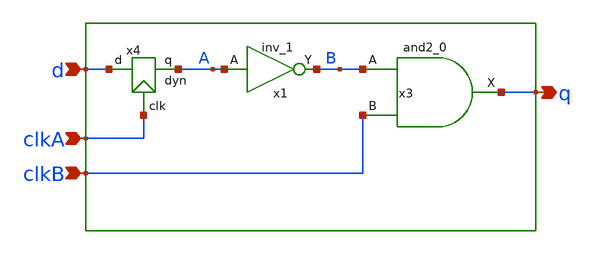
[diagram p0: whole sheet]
** sch_path: src/xe/test_cases/dyn_and.sch
**.subckt dyn_and d clkA q clkB
*.ipin d
*.ipin clkA
*.opin q
*.ipin clkB
x1 A vcc vcc vss vss B sky130_fd_sc_hd__inv_1
x3 B clkB vss vss vcc vcc q sky130_fd_sc_hd__and2_0
x4 clkA A d dyn vcc=vss vss=vss
**.ends

* expanding   symbol:  yxt/dyn.sym # of pins=3
** sym_path: src/xe/test_cases/dyn.sym
** sch_path: src/xe/test_cases/dyn.sch
.subckt dyn clk q d  vcc=vss vss=vss
*.ipin clk
*.opin q
*.ipin d
x1 net1 vcc vcc vss vss q sky130_fd_sc_hd__inv_1
XM1 net1 d net2 net3 sky130_fd_pr__nfet_01v8 L=0.15 W=1 nf=1 ad='int((nf+1)/2) * W/nf * 0.29' as='int((nf+2)/2) * W/nf * 0.29'
+ pd='2*int((nf+1)/2) * (W/nf + 0.29)' ps='2*int((nf+2)/2) * (W/nf + 0.29)' nrd='0.29 / W' nrs='0.29 / W'
+ sa=0 sb=0 sd=0 mult=1 m=1
XM2 net1 q vcc net4 sky130_fd_pr__pfet_01v8 L=0.15 W=1 nf=1 ad='int((nf+1)/2) * W/nf * 0.29' as='int((nf+2)/2) * W/nf * 0.29'
+ pd='2*int((nf+1)/2) * (W/nf + 0.29)' ps='2*int((nf+2)/2) * (W/nf + 0.29)' nrd='0.29 / W' nrs='0.29 / W'
+ sa=0 sb=0 sd=0 mult=1 m=1
XM3 net1 clk vcc net5 sky130_fd_pr__pfet_01v8 L=0.15 W=1 nf=1 ad='int((nf+1)/2) * W/nf * 0.29' as='int((nf+2)/2) * W/nf * 0.29'
+ pd='2*int((nf+1)/2) * (W/nf + 0.29)' ps='2*int((nf+2)/2) * (W/nf + 0.29)' nrd='0.29 / W' nrs='0.29 / W'
+ sa=0 sb=0 sd=0 mult=1 m=1
XM4 net2 clk vss net6 sky130_fd_pr__nfet_01v8 L=0.15 W=1 nf=1 ad='int((nf+1)/2) * W/nf * 0.29' as='int((nf+2)/2) * W/nf * 0.29'
+ pd='2*int((nf+1)/2) * (W/nf + 0.29)' ps='2*int((nf+2)/2) * (W/nf + 0.29)' nrd='0.29 / W' nrs='0.29 / W'
+ sa=0 sb=0 sd=0 mult=1 m=1
.ends

.end
